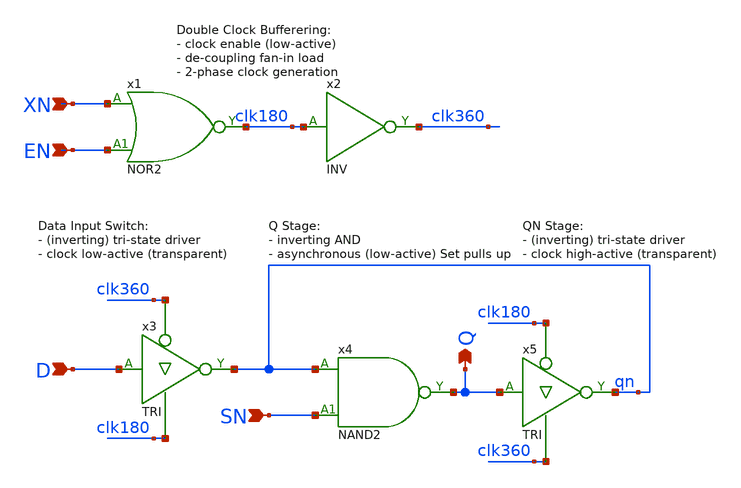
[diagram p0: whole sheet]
** sch_path: Sources/crafted/LATNES.sch
**.subckt LATNES XN D Q EN SN
*.ipin XN
*.ipin D
*.opin Q
*.ipin EN
*.ipin SN
x1 XN EN clk180 VDD GND NOR2 Wmin=1.5u Lmin=1u g=2 m=1
x2 clk180 clk360 VDD GND INV Wmin=1.5u Lmin=1u g=2 m=1
x4 qn SN Q VDD GND NAND2 Wmin=1.5u Lmin=1u g=2 m=1
x3 D clk360 clk180 qn VDD GND TRI Wmin=1.5u Lmin=1u g=2 m=1
x5 Q clk180 clk360 qn VDD GND TRI Wmin=1.5u Lmin=1u g=2 m=1
**.ends
.end
